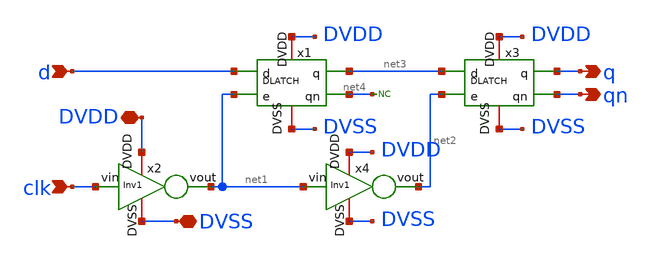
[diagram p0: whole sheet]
** sch_path: src/schematic/DLATCH/DFF.sch
**.subckt DFF d clk DVDD DVSS q qn
*.ipin d
*.ipin clk
*.iopin DVDD
*.iopin DVSS
*.opin q
*.opin qn
x1 d net3 net1 DVDD net4 DVSS DLATCH
x2 DVDD clk net1 DVSS Inv1
x3 net3 q net2 DVDD qn DVSS DLATCH
x4 DVDD net1 net2 DVSS Inv1
* noconn #net4
**.ends

* expanding   symbol:  Chipaton2026/src/schematic/DFF/DLATCH.sym # of pins=6
** sym_path: src/schematic/DLATCH/DLATCH.sym
** sch_path: src/schematic/DLATCH/DLATCH.sch
.subckt DLATCH d q e DVDD qn DVSS
*.ipin d
*.ipin e
*.iopin DVDD
*.iopin DVSS
*.opin q
*.opin qn
x1 DVDD net2 d e DVSS NAND
x2 DVDD net3 e net1 DVSS NAND
x3 DVDD q net2 qn DVSS NAND
x4 DVDD qn q net3 DVSS NAND
x5 DVDD d net1 DVSS Inv1
.ends


* expanding   symbol:  Chipaton2026/src/schematic/DFF/Inv1.sym # of pins=4
** sym_path: src/schematic/INV/Inv1.sym
** sch_path: src/schematic/INV/Inv1.sch
.subckt Inv1 DVDD vin vout DVSS
*.ipin vin
*.opin vout
*.iopin DVDD
*.iopin DVSS
XM3 vout vin DVDD DVDD pfet_03v3 L=0.3u W=1.7u nf=1 ad='int((nf+1)/2) * W/nf * 0.18u' as='int((nf+2)/2) * W/nf * 0.18u'
+ pd='2*int((nf+1)/2) * (W/nf + 0.18u)' ps='2*int((nf+2)/2) * (W/nf + 0.18u)' nrd='0.18u / W' nrs='0.18u / W'
+ sa=0 sb=0 sd=0 m=1
XM4 vout vin DVSS DVSS nfet_03v3 L=0.3u W=0.85u nf=1 ad='int((nf+1)/2) * W/nf * 0.18u' as='int((nf+2)/2) * W/nf * 0.18u'
+ pd='2*int((nf+1)/2) * (W/nf + 0.18u)' ps='2*int((nf+2)/2) * (W/nf + 0.18u)' nrd='0.18u / W' nrs='0.18u / W'
+ sa=0 sb=0 sd=0 m=1
.ends


* expanding   symbol:  src/schematic/NAND/NAND.sym # of pins=5
** sym_path: src/schematic/NAND/NAND.sym
** sch_path: src/schematic/NAND/NAND.sch
.subckt NAND DVDD vout a b DVSS
*.ipin a
*.opin vout
*.iopin DVDD
*.iopin DVSS
*.ipin b
XM3 vout a DVDD DVDD pfet_03v3 L=0.3u W=1.7u nf=1 ad='int((nf+1)/2) * W/nf * 0.18u' as='int((nf+2)/2) * W/nf * 0.18u'
+ pd='2*int((nf+1)/2) * (W/nf + 0.18u)' ps='2*int((nf+2)/2) * (W/nf + 0.18u)' nrd='0.18u / W' nrs='0.18u / W'
+ sa=0 sb=0 sd=0 m=1
XM4 vout a net1 DVSS nfet_03v3 L=0.3u W=0.85u nf=1 ad='int((nf+1)/2) * W/nf * 0.18u' as='int((nf+2)/2) * W/nf * 0.18u'
+ pd='2*int((nf+1)/2) * (W/nf + 0.18u)' ps='2*int((nf+2)/2) * (W/nf + 0.18u)' nrd='0.18u / W' nrs='0.18u / W'
+ sa=0 sb=0 sd=0 m=1
XM1 vout b DVDD DVDD pfet_03v3 L=0.3u W=1.7u nf=1 ad='int((nf+1)/2) * W/nf * 0.18u' as='int((nf+2)/2) * W/nf * 0.18u'
+ pd='2*int((nf+1)/2) * (W/nf + 0.18u)' ps='2*int((nf+2)/2) * (W/nf + 0.18u)' nrd='0.18u / W' nrs='0.18u / W'
+ sa=0 sb=0 sd=0 m=1
XM2 net1 b DVSS DVSS nfet_03v3 L=0.3u W=0.85u nf=1 ad='int((nf+1)/2) * W/nf * 0.18u' as='int((nf+2)/2) * W/nf * 0.18u'
+ pd='2*int((nf+1)/2) * (W/nf + 0.18u)' ps='2*int((nf+2)/2) * (W/nf + 0.18u)' nrd='0.18u / W' nrs='0.18u / W'
+ sa=0 sb=0 sd=0 m=1
.ends

.end
